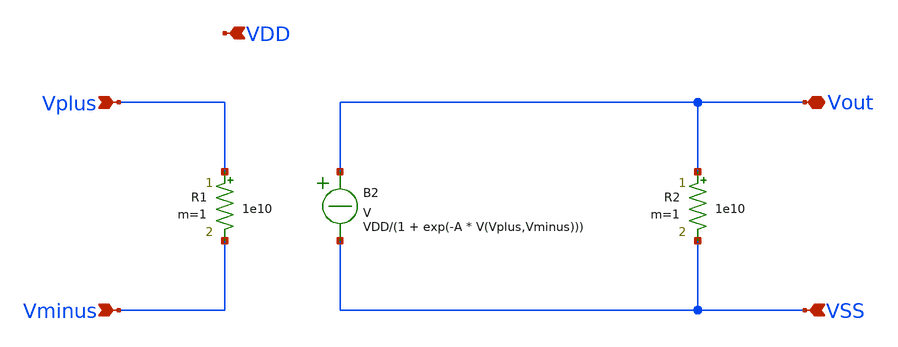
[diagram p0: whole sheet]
** sch_path: designs/libs/scratchpad/ideal_opamp/Ideal-OPAMP.sch
**.subckt Ideal-OPAMP Vplus Vminus VSS VDD Vout
*.ipin Vplus
*.ipin Vminus
*.ipin VSS
*.ipin VDD
*.iopin Vout
B2 Vout VSS V = VDD/(1 + exp(-A * V(Vplus,Vminus)))
R1 Vplus Vminus 1e10 m=1
R2 Vout VSS 1e10 m=1
**.ends
.end
